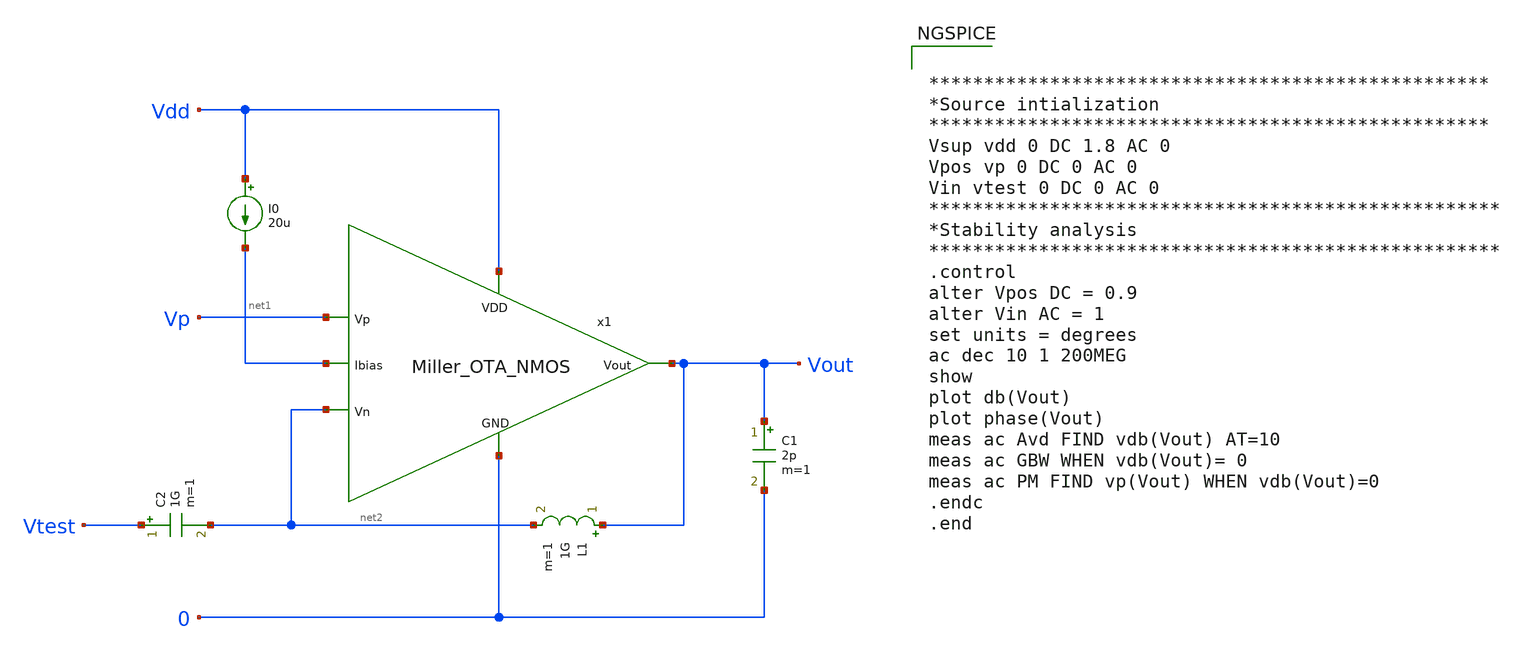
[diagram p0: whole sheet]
** sch_path: Analog_Blocks/OTA/Testbench/Miller_OTA/Transistor5v/Miller_OTA5v_meas_stability.sch
**.subckt Miller_OTA5v_meas_stability
I0 Vdd net1 20u
L1 Vout net2 1G m=1
C2 Vtest net2 1G m=1
C1 Vout 0 2p m=1
x1 Vdd net2 Vp Vout net1 0 Miller_OTA_NMOS
**** begin user architecture code


***************************************************
*Source intialization
***************************************************
Vsup vdd 0 DC 1.8 AC 0
Vpos vp 0 DC 0 AC 0
Vin vtest 0 DC 0 AC 0
****************************************************
*Stability analysis
****************************************************
.control
alter Vpos DC = 0.9
alter Vin AC = 1
set units = degrees
ac dec 10 1 200MEG
show
plot db(Vout)
plot phase(Vout)
meas ac Avd FIND vdb(Vout) AT=10
meas ac GBW WHEN vdb(Vout)= 0
meas ac PM FIND vp(Vout) WHEN vdb(Vout)=0
.endc
.end




.param mc_mm_switch=0
.param mc_pr_switch=0
.include ~/mabrains/Analog_blocks/models/sky130A/libs.ref/sky130_fd_pr/spice/sky130_fd_pr__nfet_01v8__tt.corner.spice
.include ~/mabrains/Analog_blocks/models/sky130A/libs.ref/sky130_fd_pr/spice/sky130_fd_pr__nfet_01v8_lvt__tt.corner.spice
.include ~/mabrains/Analog_blocks/models/sky130A/libs.ref/sky130_fd_pr/spice/sky130_fd_pr__pfet_01v8__tt.corner.spice
.include ~/mabrains/Analog_blocks/models/sky130A/libs.ref/sky130_fd_pr/spice/sky130_fd_pr__nfet_03v3_nvt__tt.corner.spice
.include ~/mabrains/Analog_blocks/models/sky130A/libs.ref/sky130_fd_pr/spice/sky130_fd_pr__nfet_05v0_nvt__tt.corner.spice
.include ~/mabrains/Analog_blocks/models/sky130A/libs.ref/sky130_fd_pr/spice/sky130_fd_pr__esd_nfet_01v8__tt.corner.spice
.include ~/mabrains/Analog_blocks/models/sky130A/libs.ref/sky130_fd_pr/spice/sky130_fd_pr__pfet_01v8_lvt__tt.corner.spice
.include ~/mabrains/Analog_blocks/models/sky130A/libs.ref/sky130_fd_pr/spice/sky130_fd_pr__pfet_01v8_hvt__tt.corner.spice
.include ~/mabrains/Analog_blocks/models/sky130A/libs.ref/sky130_fd_pr/spice/sky130_fd_pr__esd_pfet_g5v0d10v5__tt.corner.spice
.include ~/mabrains/Analog_blocks/models/sky130A/libs.ref/sky130_fd_pr/spice/sky130_fd_pr__pfet_g5v0d10v5__tt.corner.spice
.include ~/mabrains/Analog_blocks/models/sky130A/libs.ref/sky130_fd_pr/spice/sky130_fd_pr__pfet_g5v0d16v0__tt.corner.spice
.include ~/mabrains/Analog_blocks/models/sky130A/libs.ref/sky130_fd_pr/spice/sky130_fd_pr__nfet_g5v0d10v5__tt.corner.spice
.include ~/mabrains/Analog_blocks/models/sky130A/libs.ref/sky130_fd_pr/spice/sky130_fd_pr__nfet_g5v0d16v0__tt_discrete.corner.spice
.include ~/mabrains/Analog_blocks/models/sky130A/libs.ref/sky130_fd_pr/spice/sky130_fd_pr__esd_nfet_g5v0d10v5__tt.corner.spice
.include ~/mabrains/Analog_blocks/models/sky130A/libs.ref/sky130_fd_pr/spice/sky130_fd_pr__nfet_20v0__tt_discrete.corner.spice
.include ~/mabrains/Analog_blocks/models/sky130A/libs.ref/sky130_fd_pr/spice/sky130_fd_pr__pfet_20v0__tt_discrete.corner.spice
.include ~/mabrains/Analog_blocks/models/sky130A/libs.tech/ngspice/corners/tt/nonfet.spice
* Mismatch parameters
.include ~/mabrains/Analog_blocks/models/sky130A/libs.ref/sky130_fd_pr/spice/sky130_fd_pr__nfet_01v8__mismatch.corner.spice
.include ~/mabrains/Analog_blocks/models/sky130A/libs.ref/sky130_fd_pr/spice/sky130_fd_pr__pfet_01v8__mismatch.corner.spice
.include ~/mabrains/Analog_blocks/models/sky130A/libs.ref/sky130_fd_pr/spice/sky130_fd_pr__nfet_01v8_lvt__mismatch.corner.spice
.include ~/mabrains/Analog_blocks/models/sky130A/libs.ref/sky130_fd_pr/spice/sky130_fd_pr__pfet_01v8_lvt__mismatch.corner.spice
.include ~/mabrains/Analog_blocks/models/sky130A/libs.ref/sky130_fd_pr/spice/sky130_fd_pr__pfet_01v8_hvt__mismatch.corner.spice
.include ~/mabrains/Analog_blocks/models/sky130A/libs.ref/sky130_fd_pr/spice/sky130_fd_pr__nfet_g5v0d10v5__mismatch.corner.spice
.include ~/mabrains/Analog_blocks/models/sky130A/libs.ref/sky130_fd_pr/spice/sky130_fd_pr__pfet_g5v0d10v5__mismatch.corner.spice
.include ~/mabrains/Analog_blocks/models/sky130A/libs.ref/sky130_fd_pr/spice/sky130_fd_pr__nfet_05v0_nvt__mismatch.corner.spice
.include ~/mabrains/Analog_blocks/models/sky130A/libs.ref/sky130_fd_pr/spice/sky130_fd_pr__nfet_03v3_nvt__mismatch.corner.spice
* Resistor/Capacitor
.include ~/mabrains/Analog_blocks/models/sky130A/libs.tech/ngspice/r+c/res_typical__cap_typical.spice
.include ~/mabrains/Analog_blocks/models/sky130A/libs.tech/ngspice/r+c/res_typical__cap_typical__lin.spice
* Special cells
.include ~/mabrains/Analog_blocks/models/sky130A/libs.tech/ngspice/corners/tt/specialized_cells.spice
* All models
.include ~/mabrains/Analog_blocks/models/sky130A/libs.tech/ngspice/all.spice
* Corner
.include ~/mabrains/Analog_blocks/models/sky130A/libs.tech/ngspice/corners/tt/rf.spice



**** end user architecture code
**.ends

* expanding   symbol:
*+  /home/eslam/mabrains/Analog_blocks/Analog_Blocks/OTA/Schematic/Miller_OTA/Transistor5v/Miller_OTA_NMOS.sym # of pins=6
** sym_path: Analog_Blocks/OTA/Schematic/Miller_OTA/Transistor5v/Miller_OTA_NMOS.sym
** sch_path: Analog_Blocks/OTA/Schematic/Miller_OTA/Transistor5v/Miller_OTA_NMOS.sch
.subckt Miller_OTA_NMOS VDD Vn Vp Vout Ibias GND
*.ipin VDD
*.ipin Ibias
*.ipin Vn
*.ipin Vp
*.opin Vout
*.ipin GND
XM1 net1 Vn net3 GND sky130_fd_pr__nfet_g5v0d10v5 L=0.5 W=10 nf=1 ad='int((nf+1)/2) * W/nf * 0.29' as='int((nf+2)/2) * W/nf * 0.29'
+ pd='2*int((nf+1)/2) * (W/nf + 0.29)' ps='2*int((nf+2)/2) * (W/nf + 0.29)' nrd='0.29 / W' nrs='0.29 / W'
+ sa=0 sb=0 sd=0 mult=8 m=8
XM2 net2 Vp net3 GND sky130_fd_pr__nfet_g5v0d10v5 L=0.5 W=10 nf=1 ad='int((nf+1)/2) * W/nf * 0.29' as='int((nf+2)/2) * W/nf * 0.29'
+ pd='2*int((nf+1)/2) * (W/nf + 0.29)' ps='2*int((nf+2)/2) * (W/nf + 0.29)' nrd='0.29 / W' nrs='0.29 / W'
+ sa=0 sb=0 sd=0 mult=8 m=8
XM3 net1 net1 VDD VDD sky130_fd_pr__pfet_g5v0d10v5 L=0.5 W=5 nf=1 ad='int((nf+1)/2) * W/nf * 0.29' as='int((nf+2)/2) * W/nf * 0.29'
+ pd='2*int((nf+1)/2) * (W/nf + 0.29)' ps='2*int((nf+2)/2) * (W/nf + 0.29)' nrd='0.29 / W' nrs='0.29 / W'
+ sa=0 sb=0 sd=0 mult=4 m=4
XM4 net2 net1 VDD VDD sky130_fd_pr__pfet_g5v0d10v5 L=0.5 W=5 nf=1 ad='int((nf+1)/2) * W/nf * 0.29' as='int((nf+2)/2) * W/nf * 0.29'
+ pd='2*int((nf+1)/2) * (W/nf + 0.29)' ps='2*int((nf+2)/2) * (W/nf + 0.29)' nrd='0.29 / W' nrs='0.29 / W'
+ sa=0 sb=0 sd=0 mult=4 m=4
XM6 Vout net2 VDD VDD sky130_fd_pr__pfet_g5v0d10v5 L=0.5 W=5 nf=1 ad='int((nf+1)/2) * W/nf * 0.29' as='int((nf+2)/2) * W/nf * 0.29'
+ pd='2*int((nf+1)/2) * (W/nf + 0.29)' ps='2*int((nf+2)/2) * (W/nf + 0.29)' nrd='0.29 / W' nrs='0.29 / W'
+ sa=0 sb=0 sd=0 mult=20 m=20
XM5 net3 Ibias GND GND sky130_fd_pr__nfet_g5v0d10v5 L=1 W=3 nf=1 ad='int((nf+1)/2) * W/nf * 0.29' as='int((nf+2)/2) * W/nf * 0.29'
+ pd='2*int((nf+1)/2) * (W/nf + 0.29)' ps='2*int((nf+2)/2) * (W/nf + 0.29)' nrd='0.29 / W' nrs='0.29 / W'
+ sa=0 sb=0 sd=0 mult=8 m=8
XM8 Ibias Ibias GND GND sky130_fd_pr__nfet_g5v0d10v5 L=1 W=3 nf=1 ad='int((nf+1)/2) * W/nf * 0.29' as='int((nf+2)/2) * W/nf * 0.29'
+ pd='2*int((nf+1)/2) * (W/nf + 0.29)' ps='2*int((nf+2)/2) * (W/nf + 0.29)' nrd='0.29 / W' nrs='0.29 / W'
+ sa=0 sb=0 sd=0 mult=8 m=8
XC1 net2 Vout sky130_fd_pr__cap_mim_m3_2 W=25 L=25 MF=1 m=1
XM7 Vout Ibias GND GND sky130_fd_pr__nfet_g5v0d10v5 L=1 W=3 nf=1 ad='int((nf+1)/2) * W/nf * 0.29' as='int((nf+2)/2) * W/nf * 0.29'
+ pd='2*int((nf+1)/2) * (W/nf + 0.29)' ps='2*int((nf+2)/2) * (W/nf + 0.29)' nrd='0.29 / W' nrs='0.29 / W'
+ sa=0 sb=0 sd=0 mult=16 m=16
.ends

.end
